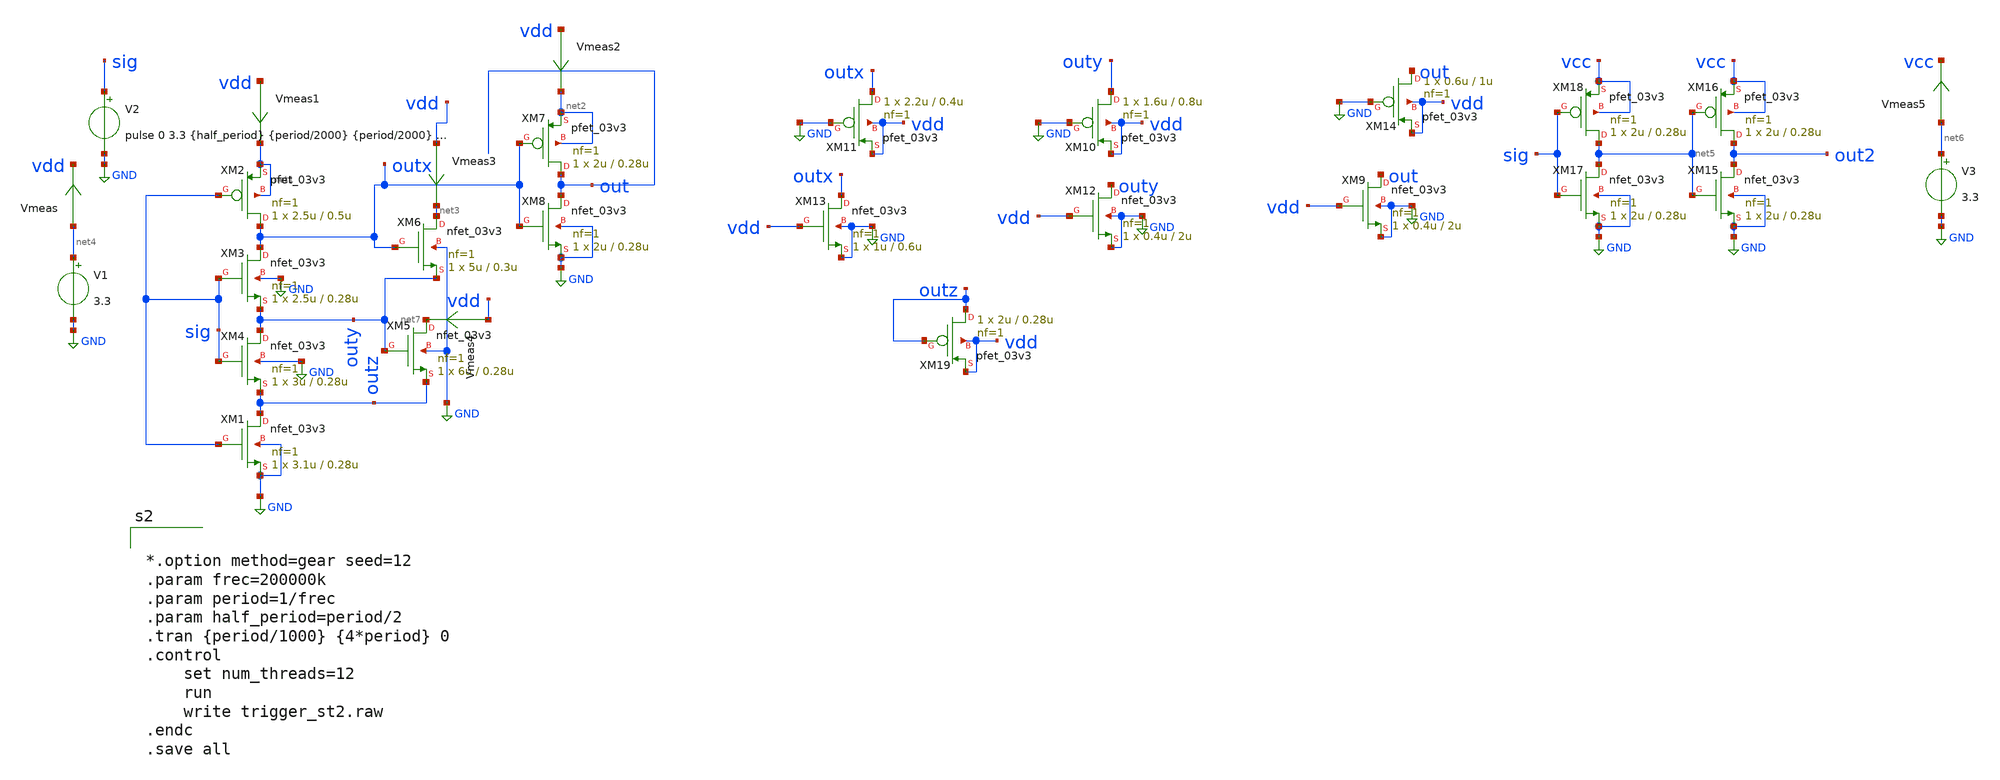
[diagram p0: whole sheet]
** sch_path: designs/libs/tb_trigger/trigger_st2.sch
**.subckt trigger_st2
XM2 outx sig net1 net1 pfet_03v3 L=0.5u W=2.5u nf=1 ad='int((nf+1)/2) * W/nf * 0.18u' as='int((nf+2)/2) * W/nf * 0.18u'
+ pd='2*int((nf+1)/2) * (W/nf + 0.18u)' ps='2*int((nf+2)/2) * (W/nf + 0.18u)' nrd='0.18u / W' nrs='0.18u / W'
+ sa=0 sb=0 sd=0 m=1
V2 sig GND pulse 0 3.3 {half_period} {period/2000} {period/2000} {half_period} {period}
V1 net4 GND 3.3
XM1 outz sig GND GND nfet_03v3 L=0.28u W=3.1u nf=1 ad='int((nf+1)/2) * W/nf * 0.18u' as='int((nf+2)/2) * W/nf * 0.18u'
+ pd='2*int((nf+1)/2) * (W/nf + 0.18u)' ps='2*int((nf+2)/2) * (W/nf + 0.18u)' nrd='0.18u / W' nrs='0.18u / W'
+ sa=0 sb=0 sd=0 m=1
XM4 outy sig outz GND nfet_03v3 L=0.28u W=3u nf=1 ad='int((nf+1)/2) * W/nf * 0.18u' as='int((nf+2)/2) * W/nf * 0.18u'
+ pd='2*int((nf+1)/2) * (W/nf + 0.18u)' ps='2*int((nf+2)/2) * (W/nf + 0.18u)' nrd='0.18u / W' nrs='0.18u / W'
+ sa=0 sb=0 sd=0 m=1
XM3 outx sig outy GND nfet_03v3 L=0.28u W=2.5u nf=1 ad='int((nf+1)/2) * W/nf * 0.18u' as='int((nf+2)/2) * W/nf * 0.18u'
+ pd='2*int((nf+1)/2) * (W/nf + 0.18u)' ps='2*int((nf+2)/2) * (W/nf + 0.18u)' nrd='0.18u / W' nrs='0.18u / W'
+ sa=0 sb=0 sd=0 m=1
XM5 net7 outy outz GND nfet_03v3 L=0.28u W=6u nf=1 ad='int((nf+1)/2) * W/nf * 0.18u' as='int((nf+2)/2) * W/nf * 0.18u'
+ pd='2*int((nf+1)/2) * (W/nf + 0.18u)' ps='2*int((nf+2)/2) * (W/nf + 0.18u)' nrd='0.18u / W' nrs='0.18u / W'
+ sa=0 sb=0 sd=0 m=1
XM6 net3 outx outy GND nfet_03v3 L=0.3u W=5u nf=1 ad='int((nf+1)/2) * W/nf * 0.18u' as='int((nf+2)/2) * W/nf * 0.18u'
+ pd='2*int((nf+1)/2) * (W/nf + 0.18u)' ps='2*int((nf+2)/2) * (W/nf + 0.18u)' nrd='0.18u / W' nrs='0.18u / W'
+ sa=0 sb=0 sd=0 m=1
XM8 out outx GND GND nfet_03v3 L=0.28u W=2u nf=1 ad='int((nf+1)/2) * W/nf * 0.18u' as='int((nf+2)/2) * W/nf * 0.18u'
+ pd='2*int((nf+1)/2) * (W/nf + 0.18u)' ps='2*int((nf+2)/2) * (W/nf + 0.18u)' nrd='0.18u / W' nrs='0.18u / W'
+ sa=0 sb=0 sd=0 m=1
XM7 out outx net2 net2 pfet_03v3 L=0.28u W=2u nf=1 ad='int((nf+1)/2) * W/nf * 0.18u' as='int((nf+2)/2) * W/nf * 0.18u'
+ pd='2*int((nf+1)/2) * (W/nf + 0.18u)' ps='2*int((nf+2)/2) * (W/nf + 0.18u)' nrd='0.18u / W' nrs='0.18u / W'
+ sa=0 sb=0 sd=0 m=1
XM9 out vdd GND GND nfet_03v3 L=2u W=0.4u nf=1 ad='int((nf+1)/2) * W/nf * 0.18u' as='int((nf+2)/2) * W/nf * 0.18u'
+ pd='2*int((nf+1)/2) * (W/nf + 0.18u)' ps='2*int((nf+2)/2) * (W/nf + 0.18u)' nrd='0.18u / W' nrs='0.18u / W'
+ sa=0 sb=0 sd=0 m=1
XM14 out GND vdd vdd pfet_03v3 L=1u W=0.6u nf=1 ad='int((nf+1)/2) * W/nf * 0.18u' as='int((nf+2)/2) * W/nf * 0.18u'
+ pd='2*int((nf+1)/2) * (W/nf + 0.18u)' ps='2*int((nf+2)/2) * (W/nf + 0.18u)' nrd='0.18u / W' nrs='0.18u / W'
+ sa=0 sb=0 sd=0 m=1
XM10 outy GND vdd vdd pfet_03v3 L=0.8u W=1.6u nf=1 ad='int((nf+1)/2) * W/nf * 0.18u' as='int((nf+2)/2) * W/nf * 0.18u'
+ pd='2*int((nf+1)/2) * (W/nf + 0.18u)' ps='2*int((nf+2)/2) * (W/nf + 0.18u)' nrd='0.18u / W' nrs='0.18u / W'
+ sa=0 sb=0 sd=0 m=1
XM11 outx GND vdd vdd pfet_03v3 L=0.4u W=2.2u nf=1 ad='int((nf+1)/2) * W/nf * 0.18u' as='int((nf+2)/2) * W/nf * 0.18u'
+ pd='2*int((nf+1)/2) * (W/nf + 0.18u)' ps='2*int((nf+2)/2) * (W/nf + 0.18u)' nrd='0.18u / W' nrs='0.18u / W'
+ sa=0 sb=0 sd=0 m=1
XM12 outy vdd GND GND nfet_03v3 L=2u W=0.4u nf=1 ad='int((nf+1)/2) * W/nf * 0.18u' as='int((nf+2)/2) * W/nf * 0.18u'
+ pd='2*int((nf+1)/2) * (W/nf + 0.18u)' ps='2*int((nf+2)/2) * (W/nf + 0.18u)' nrd='0.18u / W' nrs='0.18u / W'
+ sa=0 sb=0 sd=0 m=1
XM13 outx vdd GND GND nfet_03v3 L=0.6u W=1u nf=1 ad='int((nf+1)/2) * W/nf * 0.18u' as='int((nf+2)/2) * W/nf * 0.18u'
+ pd='2*int((nf+1)/2) * (W/nf + 0.18u)' ps='2*int((nf+2)/2) * (W/nf + 0.18u)' nrd='0.18u / W' nrs='0.18u / W'
+ sa=0 sb=0 sd=0 m=1
XM15 out2 net5 GND GND nfet_03v3 L=0.28u W=2u nf=1 ad='int((nf+1)/2) * W/nf * 0.18u' as='int((nf+2)/2) * W/nf * 0.18u'
+ pd='2*int((nf+1)/2) * (W/nf + 0.18u)' ps='2*int((nf+2)/2) * (W/nf + 0.18u)' nrd='0.18u / W' nrs='0.18u / W'
+ sa=0 sb=0 sd=0 m=1
XM16 out2 net5 vcc vcc pfet_03v3 L=0.28u W=2u nf=1 ad='int((nf+1)/2) * W/nf * 0.18u' as='int((nf+2)/2) * W/nf * 0.18u'
+ pd='2*int((nf+1)/2) * (W/nf + 0.18u)' ps='2*int((nf+2)/2) * (W/nf + 0.18u)' nrd='0.18u / W' nrs='0.18u / W'
+ sa=0 sb=0 sd=0 m=1
XM17 net5 sig GND GND nfet_03v3 L=0.28u W=2u nf=1 ad='int((nf+1)/2) * W/nf * 0.18u' as='int((nf+2)/2) * W/nf * 0.18u'
+ pd='2*int((nf+1)/2) * (W/nf + 0.18u)' ps='2*int((nf+2)/2) * (W/nf + 0.18u)' nrd='0.18u / W' nrs='0.18u / W'
+ sa=0 sb=0 sd=0 m=1
XM18 net5 sig vcc vcc pfet_03v3 L=0.28u W=2u nf=1 ad='int((nf+1)/2) * W/nf * 0.18u' as='int((nf+2)/2) * W/nf * 0.18u'
+ pd='2*int((nf+1)/2) * (W/nf + 0.18u)' ps='2*int((nf+2)/2) * (W/nf + 0.18u)' nrd='0.18u / W' nrs='0.18u / W'
+ sa=0 sb=0 sd=0 m=1
XM19 outz outz vdd vdd pfet_03v3 L=0.28u W=2u nf=1 ad='int((nf+1)/2) * W/nf * 0.18u' as='int((nf+2)/2) * W/nf * 0.18u'
+ pd='2*int((nf+1)/2) * (W/nf + 0.18u)' ps='2*int((nf+2)/2) * (W/nf + 0.18u)' nrd='0.18u / W' nrs='0.18u / W'
+ sa=0 sb=0 sd=0 m=1
Vmeas net4 vdd 0
.save i(vmeas)
Vmeas1 vdd net1 0
.save i(vmeas1)
Vmeas2 vdd net2 0
.save i(vmeas2)
Vmeas3 vdd net3 0
.save i(vmeas3)
Vmeas4 vdd net7 0
.save i(vmeas4)
V3 net6 GND 3.3
Vmeas5 net6 vcc 0
.save i(vmeas5)
**** begin user architecture code

.include $::180MCU_MODELS/design.ngspice
.lib $::180MCU_MODELS/sm141064.ngspice typical
.lib $::180MCU_MODELS/sm141064.ngspice cap_mim
.lib $::180MCU_MODELS/sm141064.ngspice res_typical
.lib $::180MCU_MODELS/sm141064.ngspice moscap_typical
.lib $::180MCU_MODELS/sm141064.ngspice mimcap_typical
.include /foss/pdks/gf180mcuD/libs.ref/gf180mcu_fd_sc_mcu9t5v0/spice/gf180mcu_fd_sc_mcu9t5v0.spice



*.option method=gear seed=12
.param frec=200000k
.param period=1/frec
.param half_period=period/2
.tran {period/1000} {4*period} 0
.control
	set num_threads=12
	run
	write trigger_st2.raw
.endc
.save all


**** end user architecture code
**.ends
.GLOBAL GND
.end
